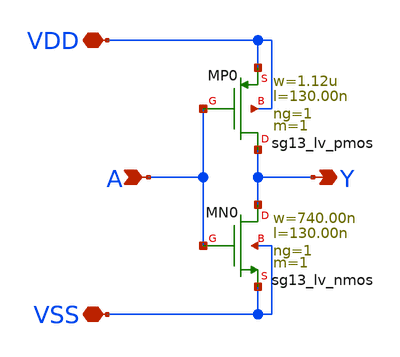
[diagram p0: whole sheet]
** sch_path: ihp-sg13g2/xschem_libs/sg13g2_stdcells/sg13g2_inv_1/schematic/sg13g2_inv_1.sch
* Copyright 2025 IHP PDK Authors
* Licensed under the Apache License, Version 2.0 (the "License");
* you may not use this file except in compliance with the License.
* You may obtain a copy of the License at
* https://www.apache.org/licenses/LICENSE-2.0
* Unless required by applicable law or agreed to in writing, software
* distributed under the License is distributed on an "AS IS" BASIS,
* WITHOUT WARRANTIES OR CONDITIONS OF ANY KIND, either express or implied.
* See the License for the specific language governing permissions and
* limitations under the License.
**.subckt sg13g2_inv_1 Y A VDD VSS
*.opin Y
*.ipin A
*.iopin VDD
*.iopin VSS
XMN0 Y A VSS VSS sg13_lv_nmos w=740.00n l=130.00n ng=1 m=1 mm_ok=1
XMP0 Y A VDD VDD sg13_lv_pmos w=1.12u l=130.00n ng=1 m=1 mm_ok=1
**.ends
.end
